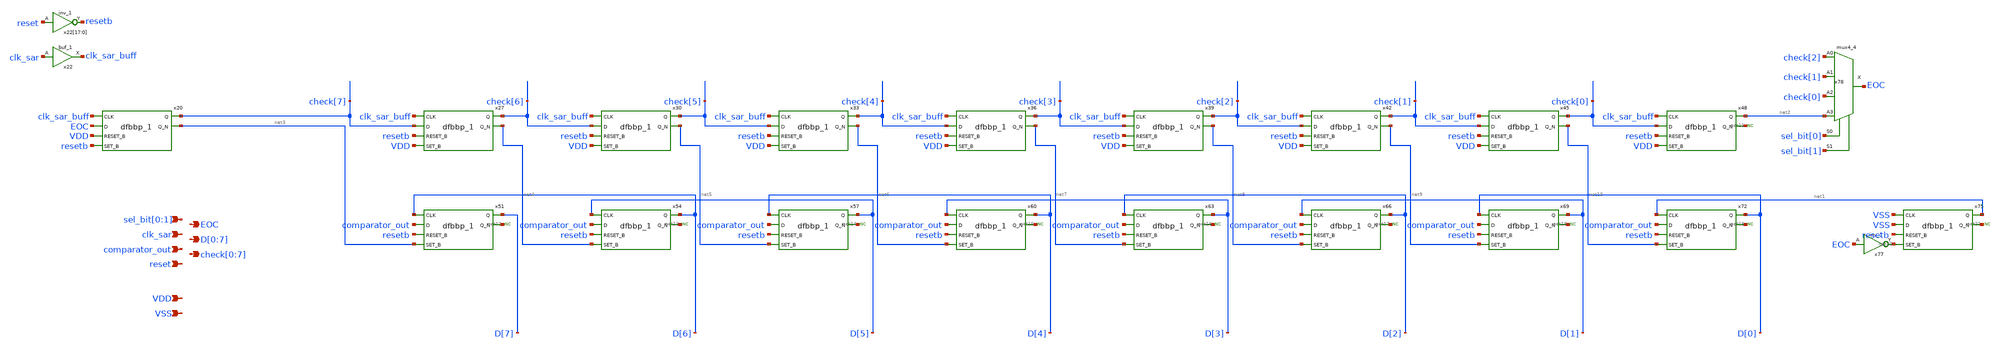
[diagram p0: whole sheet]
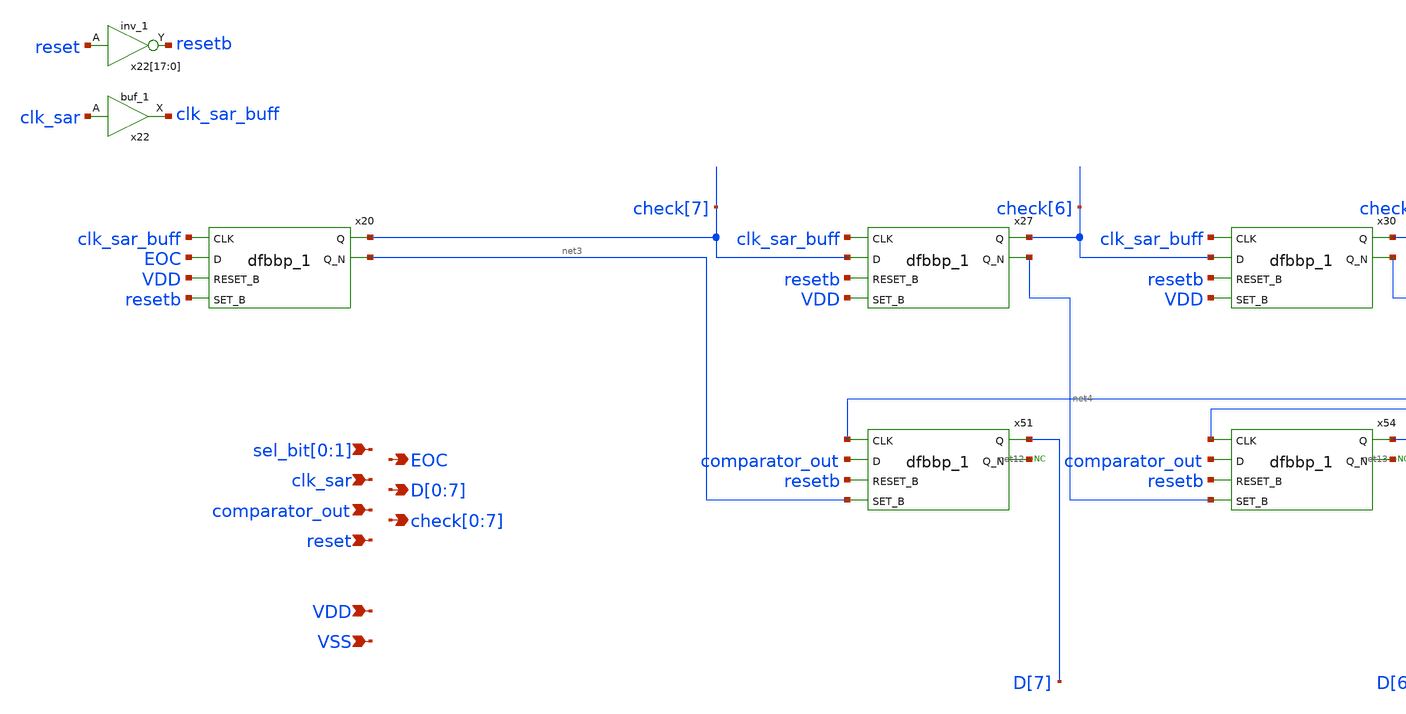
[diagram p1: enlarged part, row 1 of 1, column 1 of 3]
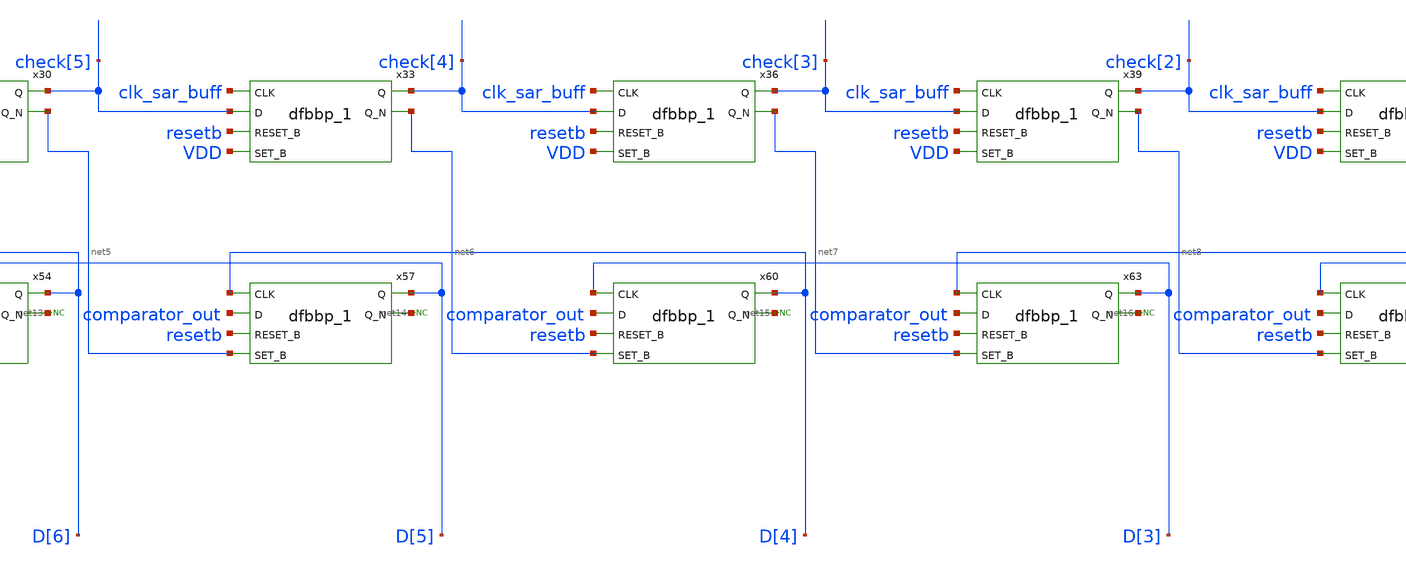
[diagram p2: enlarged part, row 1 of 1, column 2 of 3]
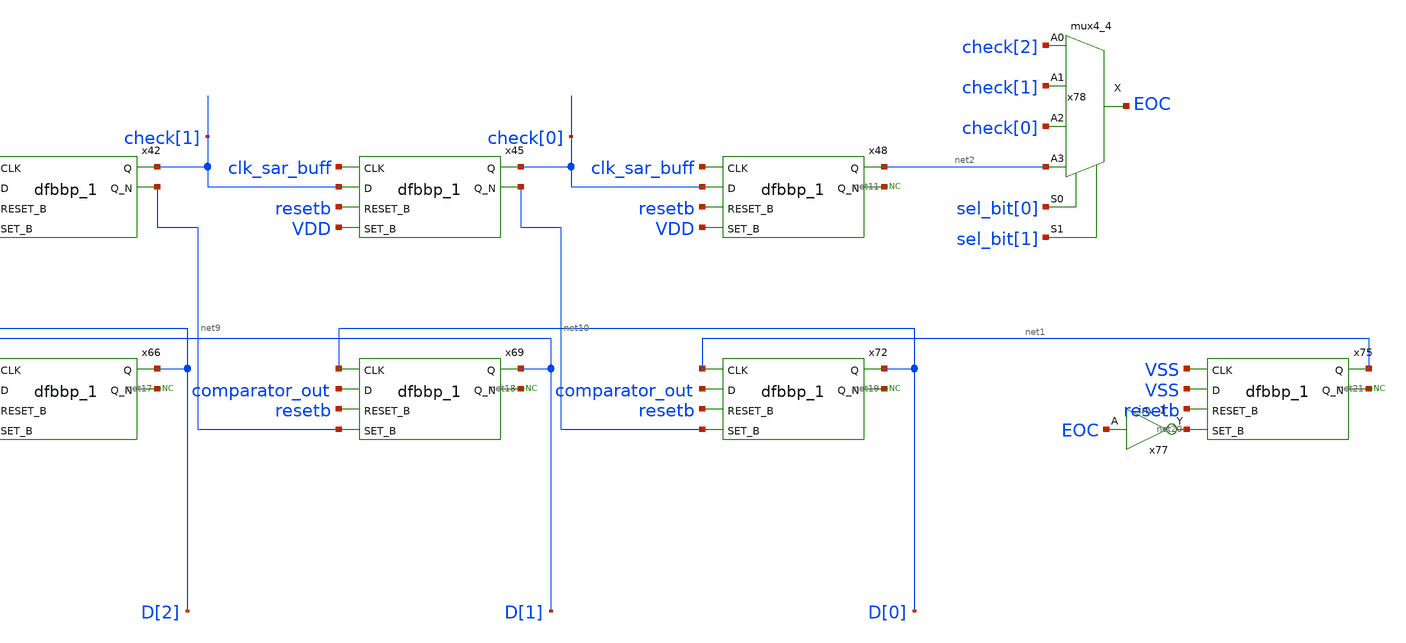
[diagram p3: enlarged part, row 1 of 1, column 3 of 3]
** sch_path: module/sar_top/sar_top/8bit_sar_logic.sch
**.subckt 8bit_sar_logic clk_sar VDD VSS comparator_out reset EOC
*+ D[0],D[1],D[2],D[3],D[4],D[5],D[6],D[7] check[0],check[1],check[2],check[3],check[4],check[5],check[6],check[7] sel_bit[0],sel_bit[1]
*.ipin clk_sar
*.ipin VDD
*.ipin VSS
*.ipin comparator_out
*.ipin reset
*.opin EOC
*.opin D[0],D[1],D[2],D[3],D[4],D[5],D[6],D[7]
*.opin check[0],check[1],check[2],check[3],check[4],check[5],check[6],check[7]
*.ipin sel_bit[0],sel_bit[1]
x20 clk_sar_buff EOC VDD resetb VGND VNB VPB VPWR check[7] net3 sky130_fd_sc_hd__dfbbp_1
x27 clk_sar_buff check[7] resetb VDD VGND VNB VPB VPWR check[6] net4 sky130_fd_sc_hd__dfbbp_1
x30 clk_sar_buff check[6] resetb VDD VGND VNB VPB VPWR check[5] net5 sky130_fd_sc_hd__dfbbp_1
x33 clk_sar_buff check[5] resetb VDD VGND VNB VPB VPWR check[4] net6 sky130_fd_sc_hd__dfbbp_1
x36 clk_sar_buff check[4] resetb VDD VGND VNB VPB VPWR check[3] net7 sky130_fd_sc_hd__dfbbp_1
x39 clk_sar_buff check[3] resetb VDD VGND VNB VPB VPWR check[2] net8 sky130_fd_sc_hd__dfbbp_1
x42 clk_sar_buff check[2] resetb VDD VGND VNB VPB VPWR check[1] net9 sky130_fd_sc_hd__dfbbp_1
x45 clk_sar_buff check[1] resetb VDD VGND VNB VPB VPWR check[0] net10 sky130_fd_sc_hd__dfbbp_1
x48 clk_sar_buff check[0] resetb VDD VGND VNB VPB VPWR net2 net11 sky130_fd_sc_hd__dfbbp_1
x51 D[6] comparator_out resetb net3 VGND VNB VPB VPWR D[7] net12 sky130_fd_sc_hd__dfbbp_1
* noconn #net12
x54 D[5] comparator_out resetb net4 VGND VNB VPB VPWR D[6] net13 sky130_fd_sc_hd__dfbbp_1
* noconn #net13
x57 D[4] comparator_out resetb net5 VGND VNB VPB VPWR D[5] net14 sky130_fd_sc_hd__dfbbp_1
* noconn #net14
x60 D[3] comparator_out resetb net6 VGND VNB VPB VPWR D[4] net15 sky130_fd_sc_hd__dfbbp_1
* noconn #net15
x63 D[2] comparator_out resetb net7 VGND VNB VPB VPWR D[3] net16 sky130_fd_sc_hd__dfbbp_1
* noconn #net16
x66 D[1] comparator_out resetb net8 VGND VNB VPB VPWR D[2] net17 sky130_fd_sc_hd__dfbbp_1
* noconn #net17
x69 D[0] comparator_out resetb net9 VGND VNB VPB VPWR D[1] net18 sky130_fd_sc_hd__dfbbp_1
* noconn #net18
x72 net1 comparator_out resetb net10 VGND VNB VPB VPWR D[0] net19 sky130_fd_sc_hd__dfbbp_1
* noconn #net19
x75 VSS VSS resetb net20 VGND VNB VPB VPWR net1 net21 sky130_fd_sc_hd__dfbbp_1
x77 EOC VGND VNB VPB VPWR net20 sky130_fd_sc_hd__inv_1
* noconn #net21
x78 check[2] check[1] check[0] net2 sel_bit[0] sel_bit[1] VGND VNB VPB VPWR EOC
+ sky130_fd_sc_hd__mux4_4
* noconn #net11
x22[17] reset VGND VNB VPB VPWR resetb sky130_fd_sc_hd__inv_1
x22[16] reset VGND VNB VPB VPWR resetb sky130_fd_sc_hd__inv_1
x22[15] reset VGND VNB VPB VPWR resetb sky130_fd_sc_hd__inv_1
x22[14] reset VGND VNB VPB VPWR resetb sky130_fd_sc_hd__inv_1
x22[13] reset VGND VNB VPB VPWR resetb sky130_fd_sc_hd__inv_1
x22[12] reset VGND VNB VPB VPWR resetb sky130_fd_sc_hd__inv_1
x22[11] reset VGND VNB VPB VPWR resetb sky130_fd_sc_hd__inv_1
x22[10] reset VGND VNB VPB VPWR resetb sky130_fd_sc_hd__inv_1
x22[9] reset VGND VNB VPB VPWR resetb sky130_fd_sc_hd__inv_1
x22[8] reset VGND VNB VPB VPWR resetb sky130_fd_sc_hd__inv_1
x22[7] reset VGND VNB VPB VPWR resetb sky130_fd_sc_hd__inv_1
x22[6] reset VGND VNB VPB VPWR resetb sky130_fd_sc_hd__inv_1
x22[5] reset VGND VNB VPB VPWR resetb sky130_fd_sc_hd__inv_1
x22[4] reset VGND VNB VPB VPWR resetb sky130_fd_sc_hd__inv_1
x22[3] reset VGND VNB VPB VPWR resetb sky130_fd_sc_hd__inv_1
x22[2] reset VGND VNB VPB VPWR resetb sky130_fd_sc_hd__inv_1
x22[1] reset VGND VNB VPB VPWR resetb sky130_fd_sc_hd__inv_1
x22[0] reset VGND VNB VPB VPWR resetb sky130_fd_sc_hd__inv_1
x22 clk_sar VGND VNB VPB VPWR clk_sar_buff sky130_fd_sc_hd__buf_1
**.ends
.end
